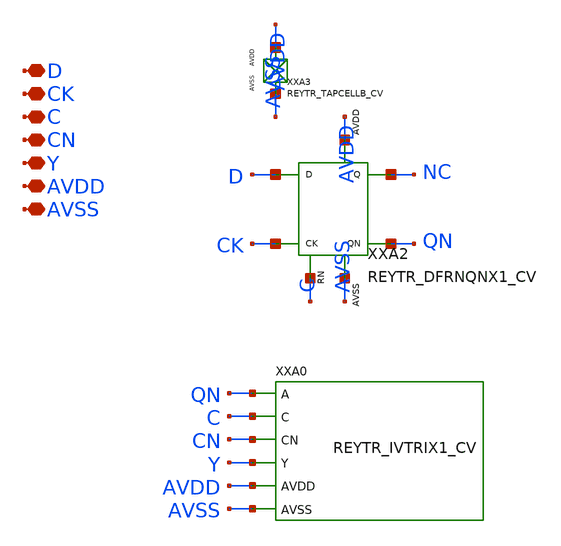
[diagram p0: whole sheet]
** sch_path: design/REY_TR_SKY130A/REYTR_DFTRIX1_CV.sch
**.subckt REYTR_DFTRIX1_CV D CK C CN Y AVDD AVSS
*.iopin D
*.iopin CK
*.iopin C
*.iopin CN
*.iopin Y
*.iopin AVDD
*.iopin AVSS
XXA3 AVDD AVSS REYTR_TAPCELLB_CV xoffset=0 yoffset=0 angle=0
XXA2 D CK C NC QN AVDD AVSS REYTR_DFRNQNX1_CV xoffset=0 yoffset=0 angle=0
XXA0 QN C CN Y AVDD AVSS REYTR_IVTRIX1_CV xoffset=0 yoffset=0 angle=0
**.ends
.end
